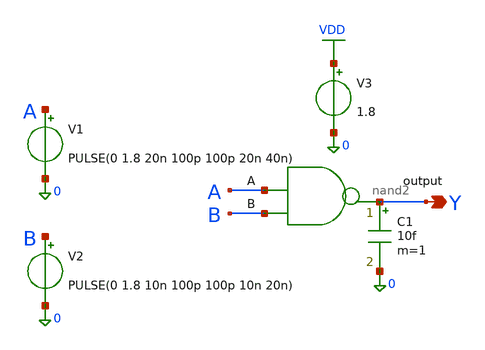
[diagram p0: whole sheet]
** sch_path: tb_nand2.sch
**.subckt tb_nand2 Y
*.opin Y
x1 A B Y nand2
V1 A 0 PULSE(0 1.8 20n 100p 100p 20n 40n)
V2 B 0 PULSE(0 1.8 10n 100p 100p 10n 20n)
V3 VDD 0 1.8
C1 Y 0 10f m=1
**** begin user architecture code
.lib /foss/pdks/sky130A/libs.tech/ngspice/sky130.lib.spice tt

.temp 27

.save all

.control

tran 10p 40n

plot v(a) v(b) v(y)

write /foss/designs/nand2_tran.raw all

.endc
**** end user architecture code
**.ends

* expanding   symbol:  nand2.sym # of pins=3
** sym_path: nand2.sym
** sch_path: nand2.sch
.subckt nand2 A B output
*.opin output
*.ipin A
*.ipin B
XM1 output A net1 0 sky130_fd_pr__nfet_01v8 L=0.15 W=3 nf=1 ad='int((1 + 1)/2) * 3 / 1 * 0.29' as='int((1 + 2)/2) * 3 / 1 * 0.29'
+ pd='2*int((1 + 1)/2) * (3 / 1 + 0.29)' ps='2*int((1 + 2)/2) * (3 / 1 + 0.29)' nrd='0.29 / 3 ' nrs='0.29 / 3 '
+ sa=0 sb=0 sd=0 mult=1 m=1
XM2 output A VDD VDD sky130_fd_pr__pfet_01v8 L=0.15 W=6 nf=1 ad='int((1 + 1)/2) * 6 / 1 * 0.29' as='int((1 + 2)/2) * 6 / 1 * 0.29'
+ pd='2*int((1 + 1)/2) * (6 / 1 + 0.29)' ps='2*int((1 + 2)/2) * (6 / 1 + 0.29)' nrd='0.29 / 6 ' nrs='0.29 / 6 '
+ sa=0 sb=0 sd=0 mult=1 m=1
XM3 output B VDD VDD sky130_fd_pr__pfet_01v8 L=0.15 W=6 nf=1 ad='int((1 + 1)/2) * 6 / 1 * 0.29' as='int((1 + 2)/2) * 6 / 1 * 0.29'
+ pd='2*int((1 + 1)/2) * (6 / 1 + 0.29)' ps='2*int((1 + 2)/2) * (6 / 1 + 0.29)' nrd='0.29 / 6 ' nrs='0.29 / 6 '
+ sa=0 sb=0 sd=0 mult=1 m=1
XM4 net1 B 0 0 sky130_fd_pr__nfet_01v8 L=0.15 W=3 nf=1 ad='int((1 + 1)/2) * 3 / 1 * 0.29' as='int((1 + 2)/2) * 3 / 1 * 0.29'
+ pd='2*int((1 + 1)/2) * (3 / 1 + 0.29)' ps='2*int((1 + 2)/2) * (3 / 1 + 0.29)' nrd='0.29 / 3 ' nrs='0.29 / 3 '
+ sa=0 sb=0 sd=0 mult=1 m=1
.ends

.GLOBAL VDD
.end
